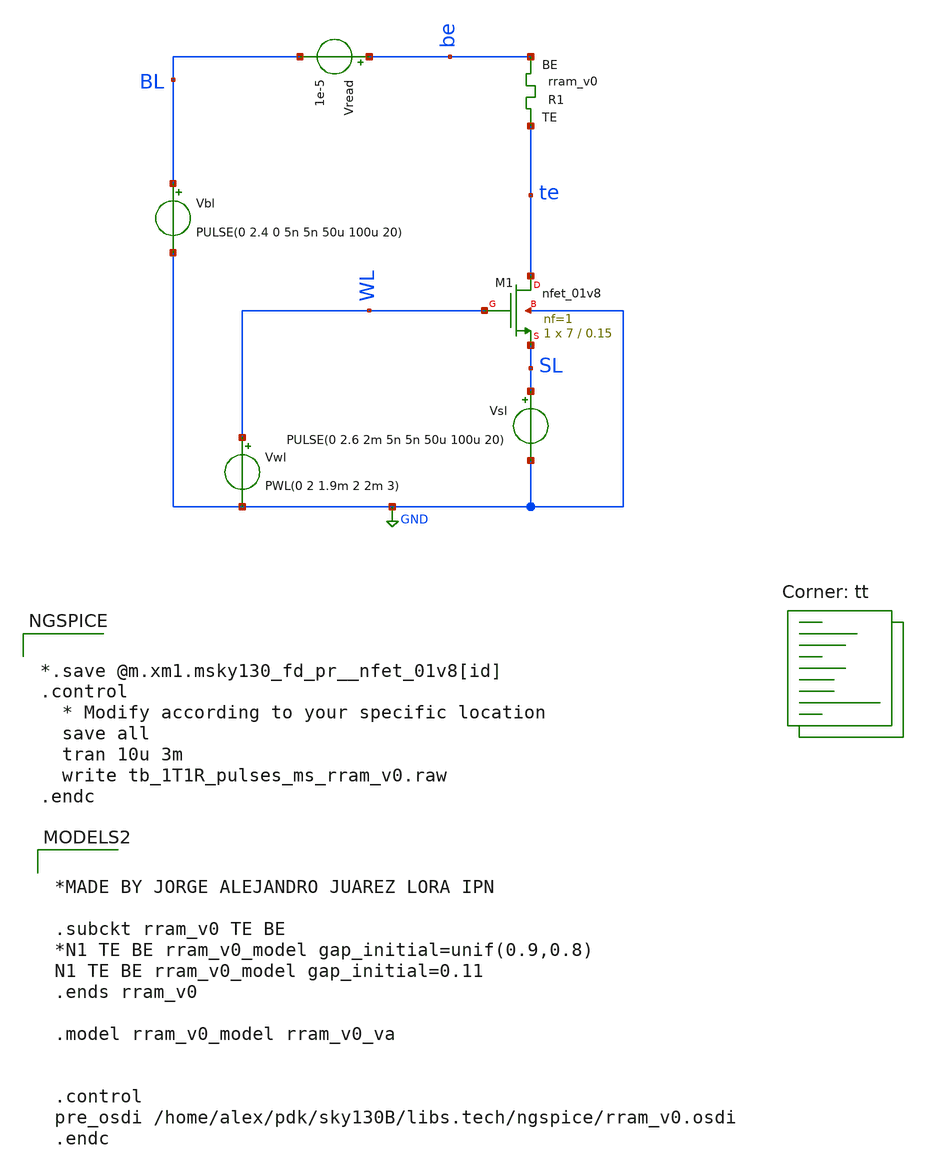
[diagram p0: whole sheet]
** sch_path: memristor_models/wellposed/tb_1T1R_pulses_ms_rram_v0.sch
**.subckt tb_1T1R_pulses_ms_rram_v0
XM1 te WL SL GND sky130_fd_pr__nfet_01v8 L=0.15 W=7 nf=1 ad='int((nf+1)/2) * W/nf * 0.29' as='int((nf+2)/2) * W/nf * 0.29'
+ pd='2*int((nf+1)/2) * (W/nf + 0.29)' ps='2*int((nf+2)/2) * (W/nf + 0.29)' nrd='0.29 / W' nrs='0.29 / W'
+ sa=0 sb=0 sd=0 mult=1 m=1
Vwl WL GND PWL(0 2 1.9m 2 2m 3)
Vbl BL GND PULSE(0 2.4 0 5n 5n 50u 100u 20)
Vread be BL 1e-5
XR1 te be rram_v0
Vsl SL GND PULSE(0 2.6 2m 5n 5n 50u 100u 20)
**** begin user architecture code


*.save @m.xm1.msky130_fd_pr__nfet_01v8[id]
.control
  * Modify according to your specific location
  save all
  tran 10u 3m
  write tb_1T1R_pulses_ms_rram_v0.raw
.endc



.lib $::SKYWATER_MODELS/sky130.lib.spice tt

*MADE BY JORGE ALEJANDRO JUAREZ LORA IPN

.subckt rram_v0 TE BE
*N1 TE BE rram_v0_model gap_initial=unif(0.9,0.8)
N1 TE BE rram_v0_model gap_initial=0.11
.ends rram_v0

.model rram_v0_model rram_v0_va


.control
pre_osdi /home/alex/pdk/sky130B/libs.tech/ngspice/rram_v0.osdi
.endc

**** end user architecture code
**.ends
.GLOBAL GND
.end
